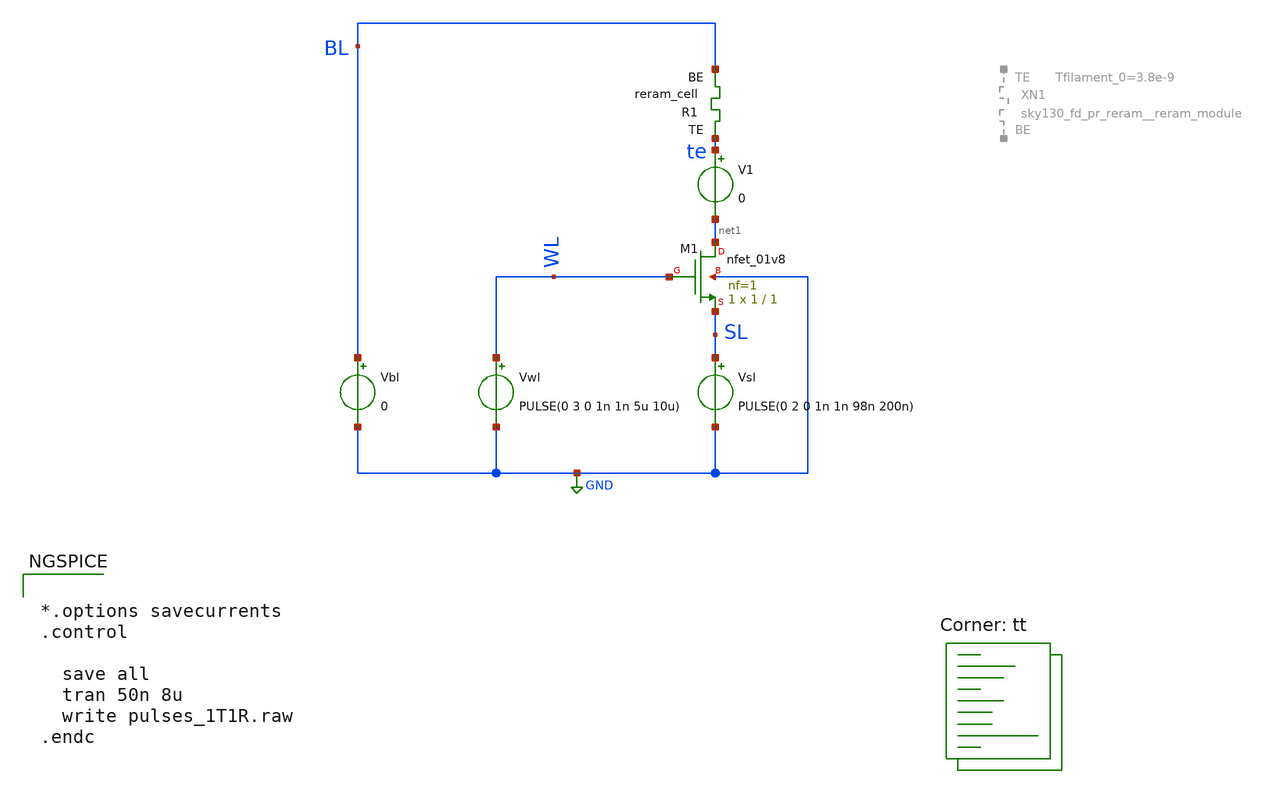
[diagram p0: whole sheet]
** sch_path: rram_test/pulses_1T1R.sch
**.subckt pulses_1T1R
XM1 net1 WL SL GND sky130_fd_pr__nfet_01v8 L=1 W=1 nf=1 ad='int((nf+1)/2) * W/nf * 0.29' as='int((nf+2)/2) * W/nf * 0.29'
+ pd='2*int((nf+1)/2) * (W/nf + 0.29)' ps='2*int((nf+2)/2) * (W/nf + 0.29)' nrd='0.29 / W' nrs='0.29 / W'
+ sa=0 sb=0 sd=0 mult=1 m=1
Vwl WL GND PULSE(0 3 0 1n 1n 5u 10u)
Vbl BL GND 0
V1 te net1 0
XR1 te BL sky130_fd_pr_reram__reram_cell Tfilament_0=3.3e-9
Vsl SL GND PULSE(0 2 0 1n 1n 98n 200n)
**** begin user architecture code


*.options savecurrents
.control

  save all
  tran 50n 8u
  write pulses_1T1R.raw
.endc



.lib $::SKYWATER_MODELS/sky130.lib.spice tt

** opencircuitdesign pdks install
.inc $::SKYWATER_MODELS/sky130_fd_pr_reram__reram_cell.spice

**** end user architecture code
**.ends
.GLOBAL GND
.end
